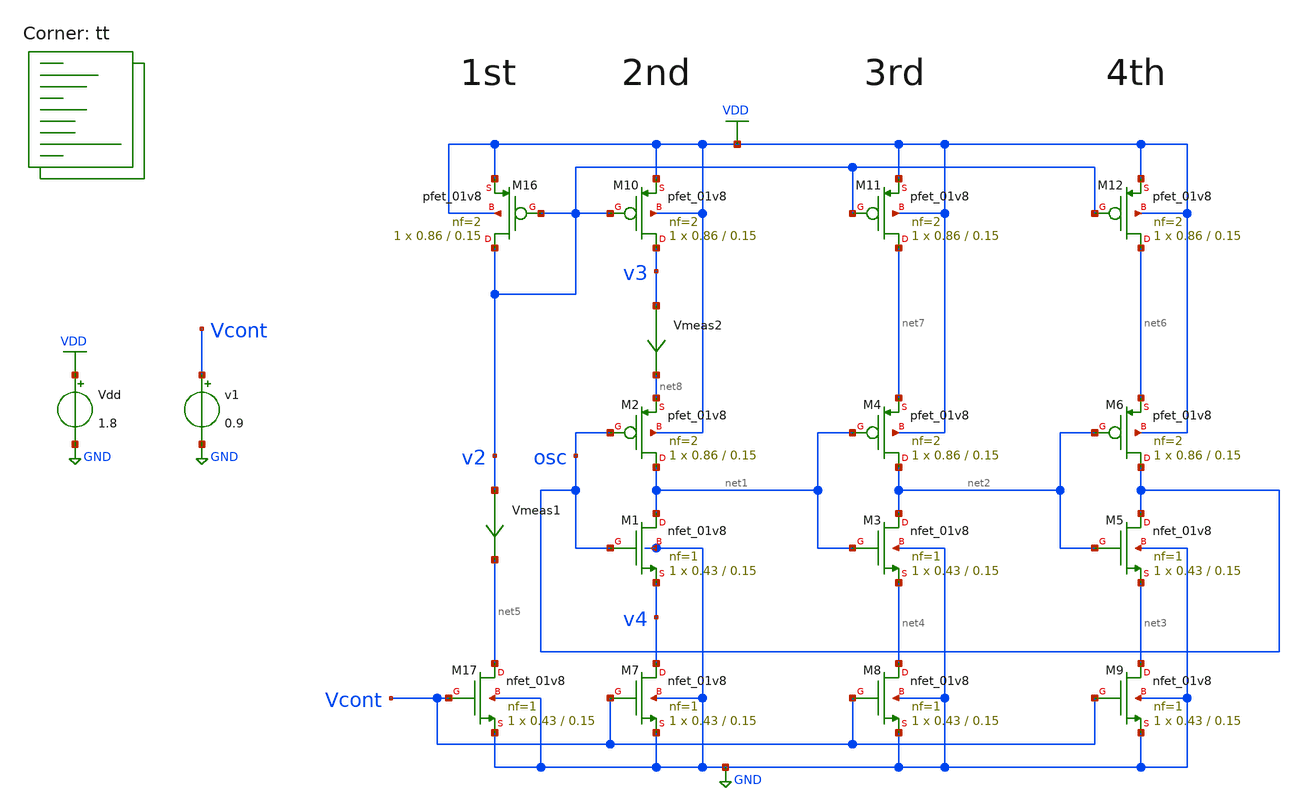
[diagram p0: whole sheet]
** sch_path: projects/pll/vco/xschem_ngspice/tb_current_starved_VCO4.sch
**.subckt tb_current_starved_VCO4
Vdd VDD GND 1.8
v1 Vcont GND 0.9
XM1 net1 osc v4 GND sky130_fd_pr__nfet_01v8 L=0.15 W=0.43 nf=1 ad='int((nf+1)/2) * W/nf * 0.29' as='int((nf+2)/2) * W/nf * 0.29'
+ pd='2*int((nf+1)/2) * (W/nf + 0.29)' ps='2*int((nf+2)/2) * (W/nf + 0.29)' nrd='0.29 / W' nrs='0.29 / W'
+ sa=0 sb=0 sd=0 mult=1 m=1
XM2 net1 osc net8 VDD sky130_fd_pr__pfet_01v8 L=0.15 W=0.86 nf=2 ad='int((nf+1)/2) * W/nf * 0.29' as='int((nf+2)/2) * W/nf * 0.29'
+ pd='2*int((nf+1)/2) * (W/nf + 0.29)' ps='2*int((nf+2)/2) * (W/nf + 0.29)' nrd='0.29 / W' nrs='0.29 / W'
+ sa=0 sb=0 sd=0 mult=1 m=1
XM3 net2 net1 net4 GND sky130_fd_pr__nfet_01v8 L=0.15 W=0.43 nf=1 ad='int((nf+1)/2) * W/nf * 0.29' as='int((nf+2)/2) * W/nf * 0.29'
+ pd='2*int((nf+1)/2) * (W/nf + 0.29)' ps='2*int((nf+2)/2) * (W/nf + 0.29)' nrd='0.29 / W' nrs='0.29 / W'
+ sa=0 sb=0 sd=0 mult=1 m=1
XM4 net2 net1 net7 VDD sky130_fd_pr__pfet_01v8 L=0.15 W=0.86 nf=2 ad='int((nf+1)/2) * W/nf * 0.29' as='int((nf+2)/2) * W/nf * 0.29'
+ pd='2*int((nf+1)/2) * (W/nf + 0.29)' ps='2*int((nf+2)/2) * (W/nf + 0.29)' nrd='0.29 / W' nrs='0.29 / W'
+ sa=0 sb=0 sd=0 mult=1 m=1
XM5 osc net2 net3 GND sky130_fd_pr__nfet_01v8 L=0.15 W=0.43 nf=1 ad='int((nf+1)/2) * W/nf * 0.29' as='int((nf+2)/2) * W/nf * 0.29'
+ pd='2*int((nf+1)/2) * (W/nf + 0.29)' ps='2*int((nf+2)/2) * (W/nf + 0.29)' nrd='0.29 / W' nrs='0.29 / W'
+ sa=0 sb=0 sd=0 mult=1 m=1
XM6 osc net2 net6 VDD sky130_fd_pr__pfet_01v8 L=0.15 W=0.86 nf=2 ad='int((nf+1)/2) * W/nf * 0.29' as='int((nf+2)/2) * W/nf * 0.29'
+ pd='2*int((nf+1)/2) * (W/nf + 0.29)' ps='2*int((nf+2)/2) * (W/nf + 0.29)' nrd='0.29 / W' nrs='0.29 / W'
+ sa=0 sb=0 sd=0 mult=1 m=1
XM7 v4 Vcont GND GND sky130_fd_pr__nfet_01v8 L=0.15 W=0.43 nf=1 ad='int((nf+1)/2) * W/nf * 0.29' as='int((nf+2)/2) * W/nf * 0.29'
+ pd='2*int((nf+1)/2) * (W/nf + 0.29)' ps='2*int((nf+2)/2) * (W/nf + 0.29)' nrd='0.29 / W' nrs='0.29 / W'
+ sa=0 sb=0 sd=0 mult=1 m=1
XM8 net4 Vcont GND GND sky130_fd_pr__nfet_01v8 L=0.15 W=0.43 nf=1 ad='int((nf+1)/2) * W/nf * 0.29' as='int((nf+2)/2) * W/nf * 0.29'
+ pd='2*int((nf+1)/2) * (W/nf + 0.29)' ps='2*int((nf+2)/2) * (W/nf + 0.29)' nrd='0.29 / W' nrs='0.29 / W'
+ sa=0 sb=0 sd=0 mult=1 m=1
XM9 net3 Vcont GND GND sky130_fd_pr__nfet_01v8 L=0.15 W=0.43 nf=1 ad='int((nf+1)/2) * W/nf * 0.29' as='int((nf+2)/2) * W/nf * 0.29'
+ pd='2*int((nf+1)/2) * (W/nf + 0.29)' ps='2*int((nf+2)/2) * (W/nf + 0.29)' nrd='0.29 / W' nrs='0.29 / W'
+ sa=0 sb=0 sd=0 mult=1 m=1
XM10 v3 v2 VDD VDD sky130_fd_pr__pfet_01v8 L=0.15 W=0.86 nf=2 ad='int((nf+1)/2) * W/nf * 0.29' as='int((nf+2)/2) * W/nf * 0.29'
+ pd='2*int((nf+1)/2) * (W/nf + 0.29)' ps='2*int((nf+2)/2) * (W/nf + 0.29)' nrd='0.29 / W' nrs='0.29 / W'
+ sa=0 sb=0 sd=0 mult=1 m=1
XM11 net7 v2 VDD VDD sky130_fd_pr__pfet_01v8 L=0.15 W=0.86 nf=2 ad='int((nf+1)/2) * W/nf * 0.29' as='int((nf+2)/2) * W/nf * 0.29'
+ pd='2*int((nf+1)/2) * (W/nf + 0.29)' ps='2*int((nf+2)/2) * (W/nf + 0.29)' nrd='0.29 / W' nrs='0.29 / W'
+ sa=0 sb=0 sd=0 mult=1 m=1
XM12 net6 v2 VDD VDD sky130_fd_pr__pfet_01v8 L=0.15 W=0.86 nf=2 ad='int((nf+1)/2) * W/nf * 0.29' as='int((nf+2)/2) * W/nf * 0.29'
+ pd='2*int((nf+1)/2) * (W/nf + 0.29)' ps='2*int((nf+2)/2) * (W/nf + 0.29)' nrd='0.29 / W' nrs='0.29 / W'
+ sa=0 sb=0 sd=0 mult=1 m=1
XM16 v2 v2 VDD VDD sky130_fd_pr__pfet_01v8 L=0.15 W=0.86 nf=2 ad='int((nf+1)/2) * W/nf * 0.29' as='int((nf+2)/2) * W/nf * 0.29'
+ pd='2*int((nf+1)/2) * (W/nf + 0.29)' ps='2*int((nf+2)/2) * (W/nf + 0.29)' nrd='0.29 / W' nrs='0.29 / W'
+ sa=0 sb=0 sd=0 mult=1 m=1
XM17 net5 Vcont GND GND sky130_fd_pr__nfet_01v8 L=0.15 W=0.43 nf=1 ad='int((nf+1)/2) * W/nf * 0.29' as='int((nf+2)/2) * W/nf * 0.29'
+ pd='2*int((nf+1)/2) * (W/nf + 0.29)' ps='2*int((nf+2)/2) * (W/nf + 0.29)' nrd='0.29 / W' nrs='0.29 / W'
+ sa=0 sb=0 sd=0 mult=1 m=1
Vmeas1 v2 net5 0
.save i(vmeas1)
Vmeas2 v3 net8 0
.save i(vmeas2)
**** begin user architecture code
.lib $::SKYWATER_MODELS/sky130.lib.spice tt



.option method=gear
.option wnflag=1

.control
  let v_cont_start = 0.0
  let v_cont_stop = 1.9

  dowhile v_cont_start <= v_cont_stop
    alter v1 $&v_cont_start
    save v(osc) v(vcont) v(v2) v(v3) v(v4)
    tran 2ps 30ns
    remzerovec
    write tb_current_starved_VCO4_{$&v_cont_start}.raw
    let filename = v_cont_start * 100
    wrdata /foss/designs/my_design/projects/pll/vco/xschem_ngspice/tb_current_starved_VCO4_{$&filename}.txt
+ v(osc)
    set appendwrite
    reset
    let v_cont_start = v_cont_start + 0.1
  end
.endc



**** end user architecture code
**.ends
.GLOBAL GND
.GLOBAL VDD
.end
